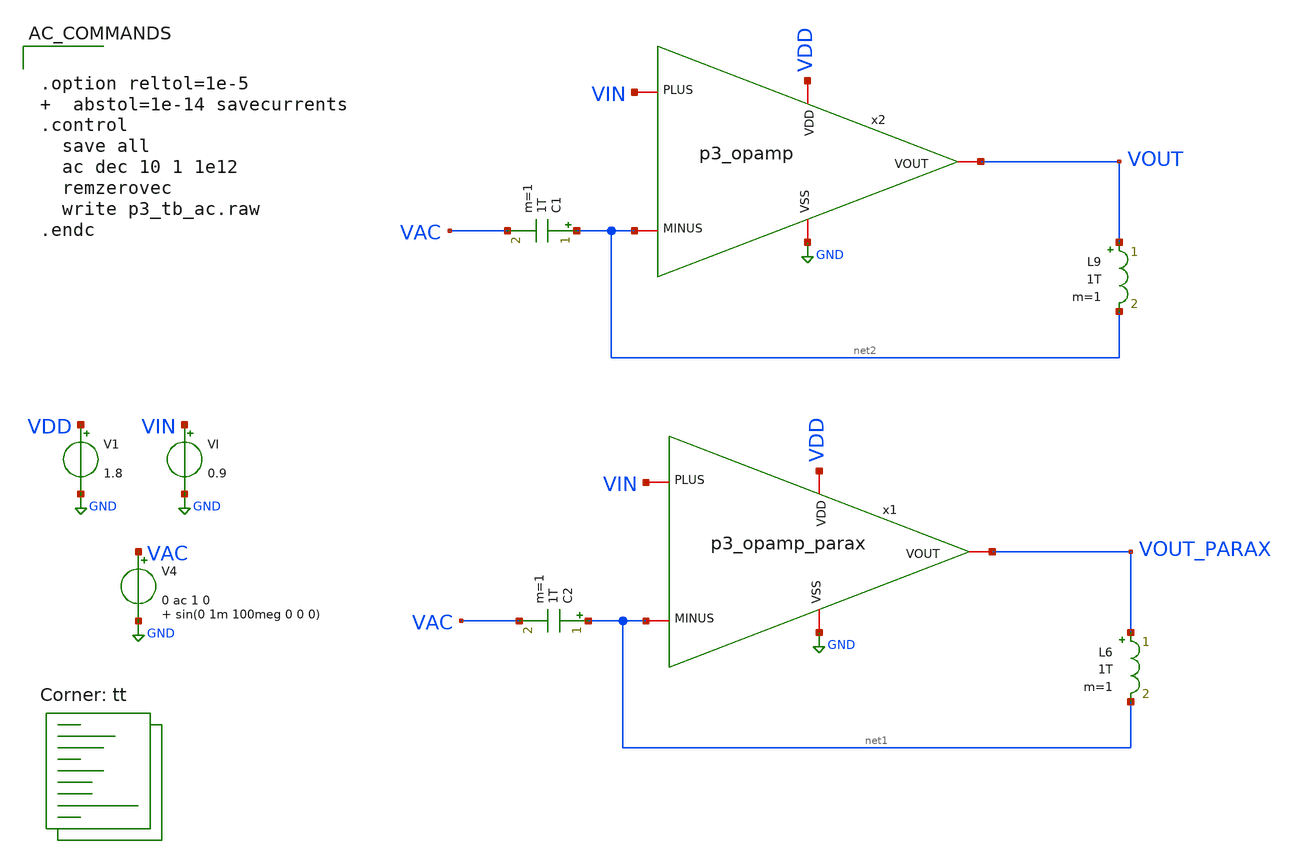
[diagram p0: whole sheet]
** sch_path: xschem/p3_tb_ac.sch
**.subckt p3_tb_ac
V1 VDD GND 1.8
VI VIN GND 0.9
C2 net1 VAC 1T m=1
L6 VOUT_PARAX net1 1T m=1
V4 VAC GND 0 ac 1 0 sin(0 1m 100meg 0 0 0)
C1 net2 VAC 1T m=1
L9 VOUT net2 1T m=1
x2 VDD net2 VIN VOUT GND p3_opamp
x1 VDD net1 VIN VOUT_PARAX GND p3_opamp_parax
**** begin user architecture code
.lib $::SKYWATER_MODELS/sky130.lib.spice tt


.option reltol=1e-5   abstol=1e-14 savecurrents
.control
  save all
  ac dec 10 1 1e12
  remzerovec
  write p3_tb_ac.raw
.endc


**** end user architecture code
**.ends

* expanding   symbol:  p3_opamp.sym # of pins=5
** sym_path: p3_opamp.sym
** sch_path: p3_opamp.sch
.subckt p3_opamp VDD MINUS PLUS VOUT VSS
*.iopin VDD
*.iopin VSS
*.iopin PLUS
*.iopin MINUS
*.iopin VOUT
XM3 VX VBIAS VSS VSS sky130_fd_pr__nfet_01v8 L=2 W=4 nf=1 ad='int((nf+1)/2) * W/nf * 0.29' as='int((nf+2)/2) * W/nf * 0.29'
+ pd='2*int((nf+1)/2) * (W/nf + 0.29)' ps='2*int((nf+2)/2) * (W/nf + 0.29)' nrd='0.29 / W' nrs='0.29 / W'
+ sa=0 sb=0 sd=0 mult=1 m=1
XM6 VBIAS VBIAS VSS VSS sky130_fd_pr__nfet_01v8 L=2 W=4 nf=1 ad='int((nf+1)/2) * W/nf * 0.29' as='int((nf+2)/2) * W/nf * 0.29'
+ pd='2*int((nf+1)/2) * (W/nf + 0.29)' ps='2*int((nf+2)/2) * (W/nf + 0.29)' nrd='0.29 / W' nrs='0.29 / W'
+ sa=0 sb=0 sd=0 mult=1 m=1
XM7 VOUT VBIAS VSS VSS sky130_fd_pr__nfet_01v8 L=2 W=7 nf=1 ad='int((nf+1)/2) * W/nf * 0.29' as='int((nf+2)/2) * W/nf * 0.29'
+ pd='2*int((nf+1)/2) * (W/nf + 0.29)' ps='2*int((nf+2)/2) * (W/nf + 0.29)' nrd='0.29 / W' nrs='0.29 / W'
+ sa=0 sb=0 sd=0 mult=1 m=1
XM8 VOUT V1 VDD VDD sky130_fd_pr__pfet_01v8 L=2 W=80 nf=1 ad='int((nf+1)/2) * W/nf * 0.29' as='int((nf+2)/2) * W/nf * 0.29'
+ pd='2*int((nf+1)/2) * (W/nf + 0.29)' ps='2*int((nf+2)/2) * (W/nf + 0.29)' nrd='0.29 / W' nrs='0.29 / W'
+ sa=0 sb=0 sd=0 mult=4 m=4
XR1 VBIAS VDD VSS sky130_fd_pr__res_xhigh_po_0p35 L=2.8 mult=1 m=1
XM2 V2 MINUS VX VSS sky130_fd_pr__nfet_01v8_lvt L=0.5 W=2.5 nf=1 ad='int((nf+1)/2) * W/nf * 0.29' as='int((nf+2)/2) * W/nf * 0.29'
+ pd='2*int((nf+1)/2) * (W/nf + 0.29)' ps='2*int((nf+2)/2) * (W/nf + 0.29)' nrd='0.29 / W' nrs='0.29 / W'
+ sa=0 sb=0 sd=0 mult=1 m=1
XM1 V1 PLUS VX VSS sky130_fd_pr__nfet_01v8_lvt L=0.5 W=2.5 nf=1 ad='int((nf+1)/2) * W/nf * 0.29' as='int((nf+2)/2) * W/nf * 0.29'
+ pd='2*int((nf+1)/2) * (W/nf + 0.29)' ps='2*int((nf+2)/2) * (W/nf + 0.29)' nrd='0.29 / W' nrs='0.29 / W'
+ sa=0 sb=0 sd=0 mult=1 m=1
XM4 V2 V2 VDD VDD sky130_fd_pr__pfet_01v8_lvt L=2 W=6 nf=1 ad='int((nf+1)/2) * W/nf * 0.29' as='int((nf+2)/2) * W/nf * 0.29'
+ pd='2*int((nf+1)/2) * (W/nf + 0.29)' ps='2*int((nf+2)/2) * (W/nf + 0.29)' nrd='0.29 / W' nrs='0.29 / W'
+ sa=0 sb=0 sd=0 mult=1 m=1
XM5 V1 V2 VDD VDD sky130_fd_pr__pfet_01v8_lvt L=2 W=6 nf=1 ad='int((nf+1)/2) * W/nf * 0.29' as='int((nf+2)/2) * W/nf * 0.29'
+ pd='2*int((nf+1)/2) * (W/nf + 0.29)' ps='2*int((nf+2)/2) * (W/nf + 0.29)' nrd='0.29 / W' nrs='0.29 / W'
+ sa=0 sb=0 sd=0 mult=1 m=1
.ends


* expanding   symbol:  p3_opamp_parax.sym # of pins=5
** sym_path: p3_opamp.sym
.include [file normalize ../mag/p3_opamp.sim.spice]
.GLOBAL GND
.end
